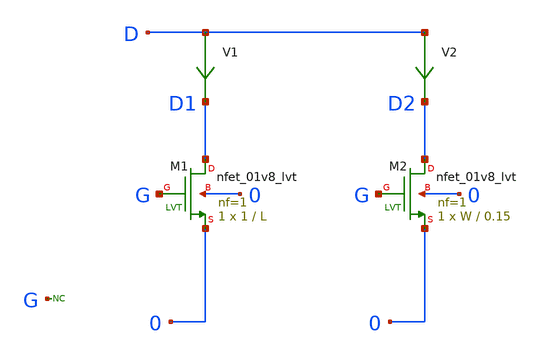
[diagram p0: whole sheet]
** sch_path: sky130A/xschem_libs/sky130_tests_ase/test_nmos_sizes/schematic/test_nmos_sizes.sch
* Copyright 2021 Stefan Frederik Schippers
* Licensed under the Apache License, Version 2.0 (the "License");
* you may not use this file except in compliance with the License.
* You may obtain a copy of the License at
* https://www.apache.org/licenses/LICENSE-2.0
* Unless required by applicable law or agreed to in writing, software
* distributed under the License is distributed on an "AS IS" BASIS,
* WITHOUT WARRANTIES OR CONDITIONS OF ANY KIND, either express or implied.
* See the License for the specific language governing permissions and
* limitations under the License.
**.subckt test_nmos_sizes
XM1 D1 G 0 0 sky130_fd_pr__nfet_01v8_lvt L=L W=1 nf=1 ad='int((1 + 1)/2) * 1 / 1 * 0.29' as='int((1 + 2)/2) * 1 / 1 * 0.29'
+ pd='2*int((1 + 1)/2) * (1 / 1 + 0.29)' ps='2*int((1 + 2)/2) * (1 / 1 + 0.29)' nrd='0.29 / 1 ' nrs='0.29 / 1 '
+ sa=0 sb=0 sd=0 mult=1 m=1
XM2 D2 G 0 0 sky130_fd_pr__nfet_01v8_lvt L=0.15 W=W nf=1 ad='int((1 + 1)/2) * W / 1 * 0.29' as='int((1 + 2)/2) * W / 1 * 0.29'
+ pd='2*int((1 + 1)/2) * (W / 1 + 0.29)' ps='2*int((1 + 2)/2) * (W / 1 + 0.29)' nrd='0.29 / W ' nrs='0.29 / W '
+ sa=0 sb=0 sd=0 mult=1 m=1
V2 D D2 0
.save i(v2)
V1 D D1 0
.save i(v1)
* noconn G
**.ends
**** begin user architecture code


vd d 0 0
vg g 0 0


**** end user architecture code
.end
